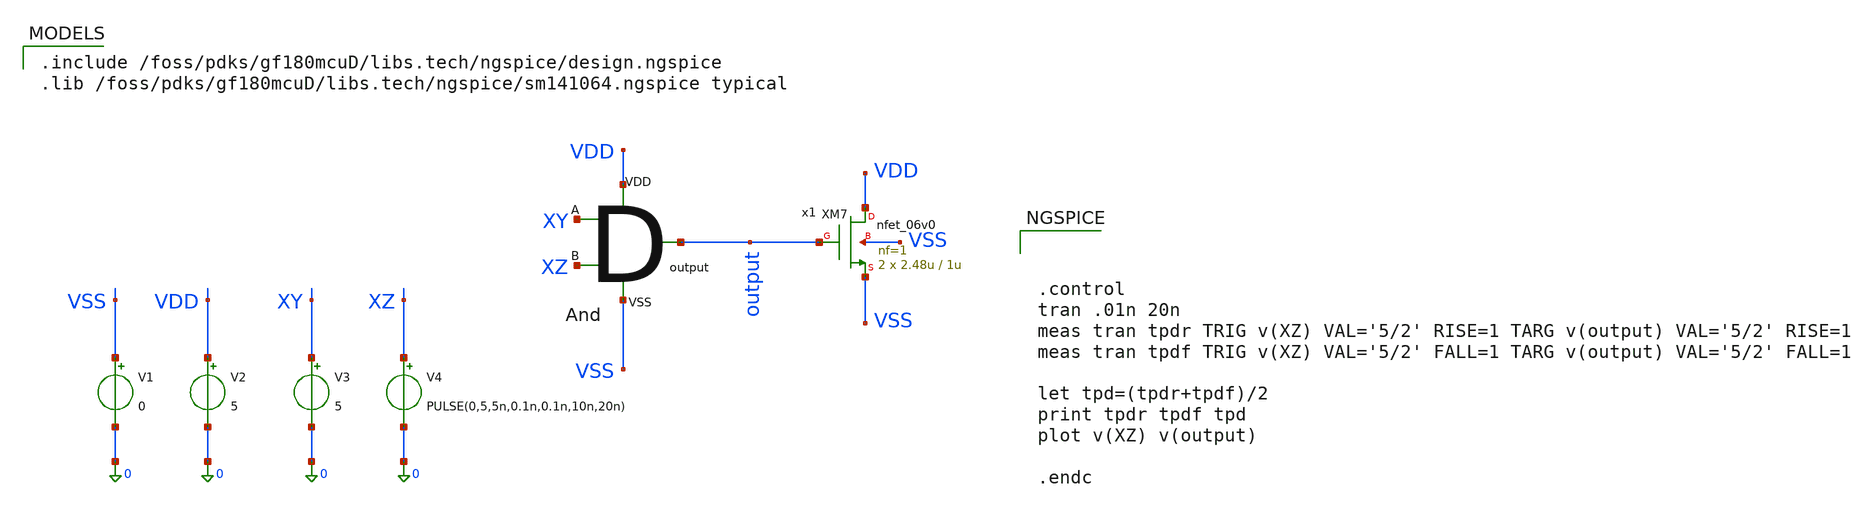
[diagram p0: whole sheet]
** sch_path: activities/opamp3AKAM/xDelayTB2.sch
**.subckt xDelayTB2
V1 VSS 0 0
V2 VDD 0 5
V3 XY 0 5
V4 XZ 0 PULSE(0,5,5n,0.1n,0.1n,10n,20n)
x1 XY VDD XZ output VSS andGate
XM7 VDD output VSS VSS nfet_06v0 L=1u W=2.48u nf=1 ad='int((nf+1)/2) * W/nf * 0.18u' as='int((nf+2)/2) * W/nf * 0.18u'
+ pd='2*int((nf+1)/2) * (W/nf + 0.18u)' ps='2*int((nf+2)/2) * (W/nf + 0.18u)' nrd='0.18u / W' nrs='0.18u / W'
+ sa=0 sb=0 sd=0 m=2
**** begin user architecture code

.include /foss/pdks/gf180mcuD/libs.tech/ngspice/design.ngspice
.lib /foss/pdks/gf180mcuD/libs.tech/ngspice/sm141064.ngspice typical




.control
tran .01n 20n
meas tran tpdr TRIG v(XZ) VAL='5/2' RISE=1 TARG v(output) VAL='5/2' RISE=1
meas tran tpdf TRIG v(XZ) VAL='5/2' FALL=1 TARG v(output) VAL='5/2' FALL=1

let tpd=(tpdr+tpdf)/2
print tpdr tpdf tpd
plot v(XZ) v(output)

.endc


**** end user architecture code
**.ends
.end
